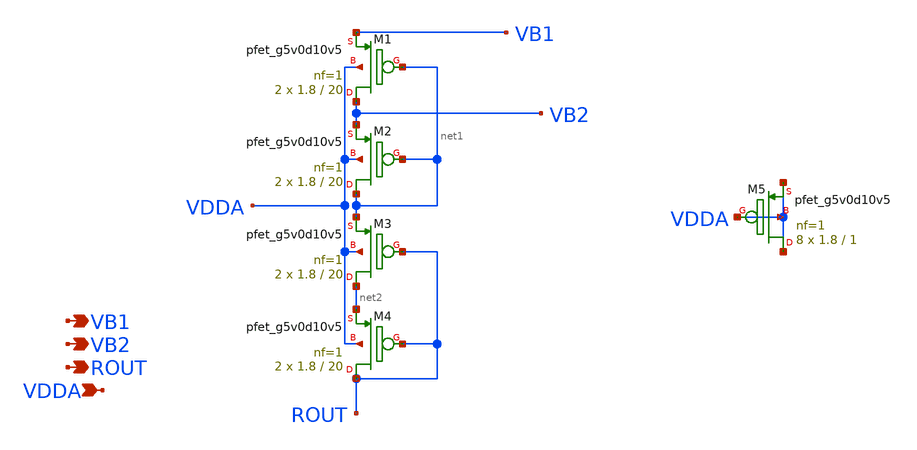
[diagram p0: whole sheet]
** sch_path: xschem/cm_pcell3.sch
**.subckt cm_pcell3 VDDA VB1 VB2 ROUT
*.ipin VDDA
*.opin VB1
*.opin VB2
*.opin ROUT
XM1 VB2 net1 VB1 VDDA sky130_fd_pr__pfet_g5v0d10v5 L=20 W=1.8 nf=1 ad='int((nf+1)/2) * W/nf * 0.29' as='int((nf+2)/2) * W/nf * 0.29'
+ pd='2*int((nf+1)/2) * (W/nf + 0.29)' ps='2*int((nf+2)/2) * (W/nf + 0.29)' nrd='0.29 / W' nrs='0.29 / W'
+ sa=0 sb=0 sd=0 mult=2 m=2
XM2 net1 net1 VB2 VDDA sky130_fd_pr__pfet_g5v0d10v5 L=20 W=1.8 nf=1 ad='int((nf+1)/2) * W/nf * 0.29'
+ as='int((nf+2)/2) * W/nf * 0.29' pd='2*int((nf+1)/2) * (W/nf + 0.29)' ps='2*int((nf+2)/2) * (W/nf + 0.29)'
+ nrd='0.29 / W' nrs='0.29 / W' sa=0 sb=0 sd=0 mult=2 m=2
XM3 net2 ROUT net1 VDDA sky130_fd_pr__pfet_g5v0d10v5 L=20 W=1.8 nf=1 ad='int((nf+1)/2) * W/nf * 0.29'
+ as='int((nf+2)/2) * W/nf * 0.29' pd='2*int((nf+1)/2) * (W/nf + 0.29)' ps='2*int((nf+2)/2) * (W/nf + 0.29)'
+ nrd='0.29 / W' nrs='0.29 / W' sa=0 sb=0 sd=0 mult=2 m=2
XM4 ROUT ROUT net2 VDDA sky130_fd_pr__pfet_g5v0d10v5 L=20 W=1.8 nf=1 ad='int((nf+1)/2) * W/nf * 0.29'
+ as='int((nf+2)/2) * W/nf * 0.29' pd='2*int((nf+1)/2) * (W/nf + 0.29)' ps='2*int((nf+2)/2) * (W/nf + 0.29)'
+ nrd='0.29 / W' nrs='0.29 / W' sa=0 sb=0 sd=0 mult=2 m=2
XM5 VDDA VDDA VDDA VDDA sky130_fd_pr__pfet_g5v0d10v5 L=1 W=1.8 nf=1 ad='int((nf+1)/2) * W/nf * 0.29'
+ as='int((nf+2)/2) * W/nf * 0.29' pd='2*int((nf+1)/2) * (W/nf + 0.29)' ps='2*int((nf+2)/2) * (W/nf + 0.29)'
+ nrd='0.29 / W' nrs='0.29 / W' sa=0 sb=0 sd=0 mult=8 m=8
**.ends
.end
